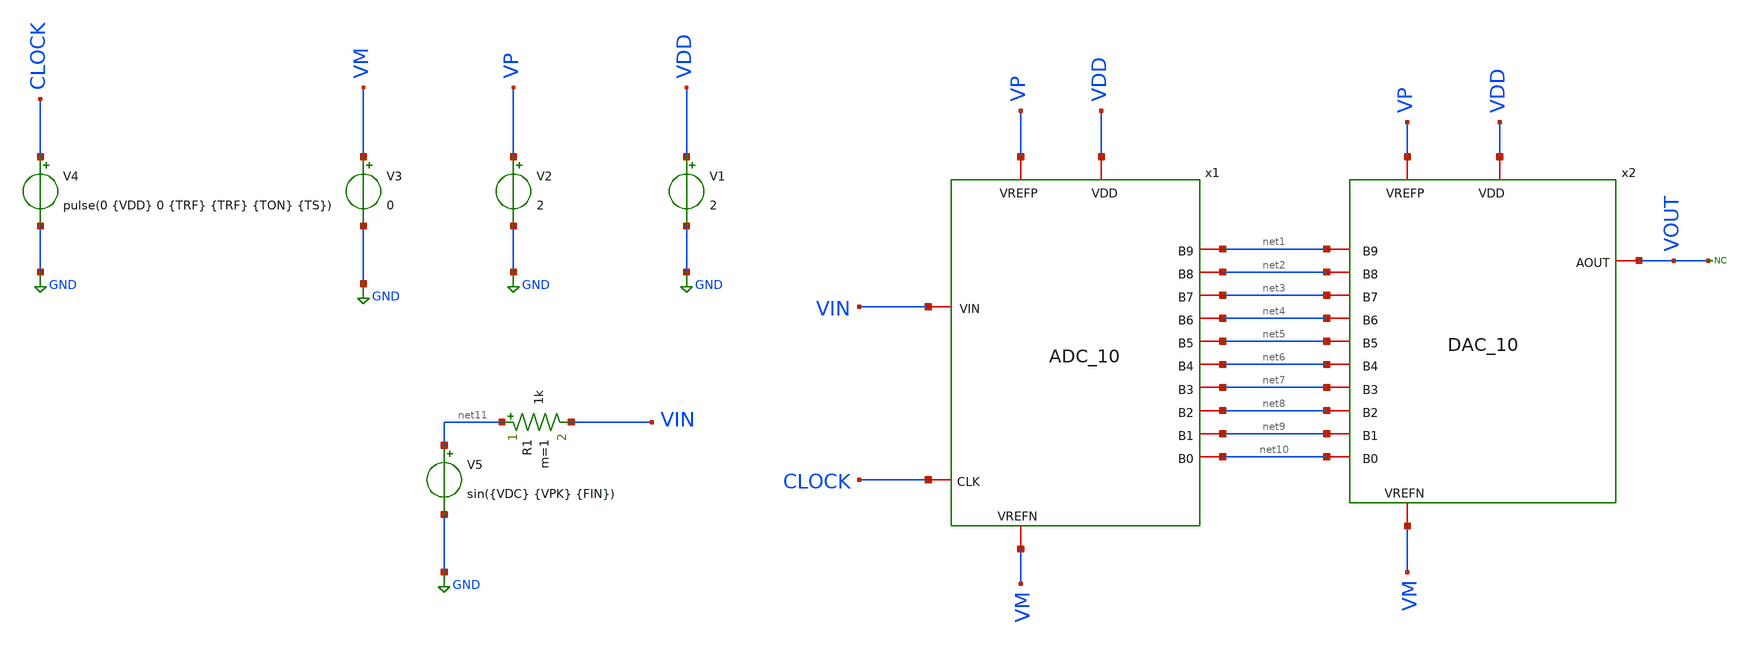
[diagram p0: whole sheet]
** sch_path: Designs/lab2_part2.sch
**.subckt lab2_part2
x1 VM VP VDD VIN CLOCK net10 net9 net7 net8 net6 net5 net3 net4 net2 net1 ADC_10
x2 VP VDD VOUT net5 net6 net2 net9 net4 net10 net8 net7 net3 net1 VM DAC_10
V1 VDD GND 2
V2 VP GND 2
V3 VM GND 0
V4 CLOCK GND pulse(0 {VDD} 0 {TRF} {TRF} {TON} {TS})
V5 net11 GND sin({VDC} {VPK} {FIN})
R1 net11 VIN 1k m=1
* noconn VOUT
**** begin user architecture code


*Required model for the switch
.model SWITCH1 sw vt=0
*These are the values of the parameters to be used
.param TS=1u
.param CH=1p CP={0.1*CH} RSIG=1k TON={0.4*TS} TRF=1n NCYC=5 NFFT=256 FIN={(NCYC/NFFT)/TS}
.param VDD=2 VDC={VDD/2} VCM={VDD/2} VPK={VDD/4} TDROP={0.5/FIN} TSTOP={(NCYC/FIN)+TDROP}
*Analysis setup and control statements

.tran 25n {TSTOP} {TDROP}
*save all voltages and currents
.save all
*options for an accurate precision output and to allow raw files to be ascii
.options filetype=ascii
.options reltol=1u vntol=1u abstol=1p


**** end user architecture code
**.ends
.GLOBAL GND
.end
